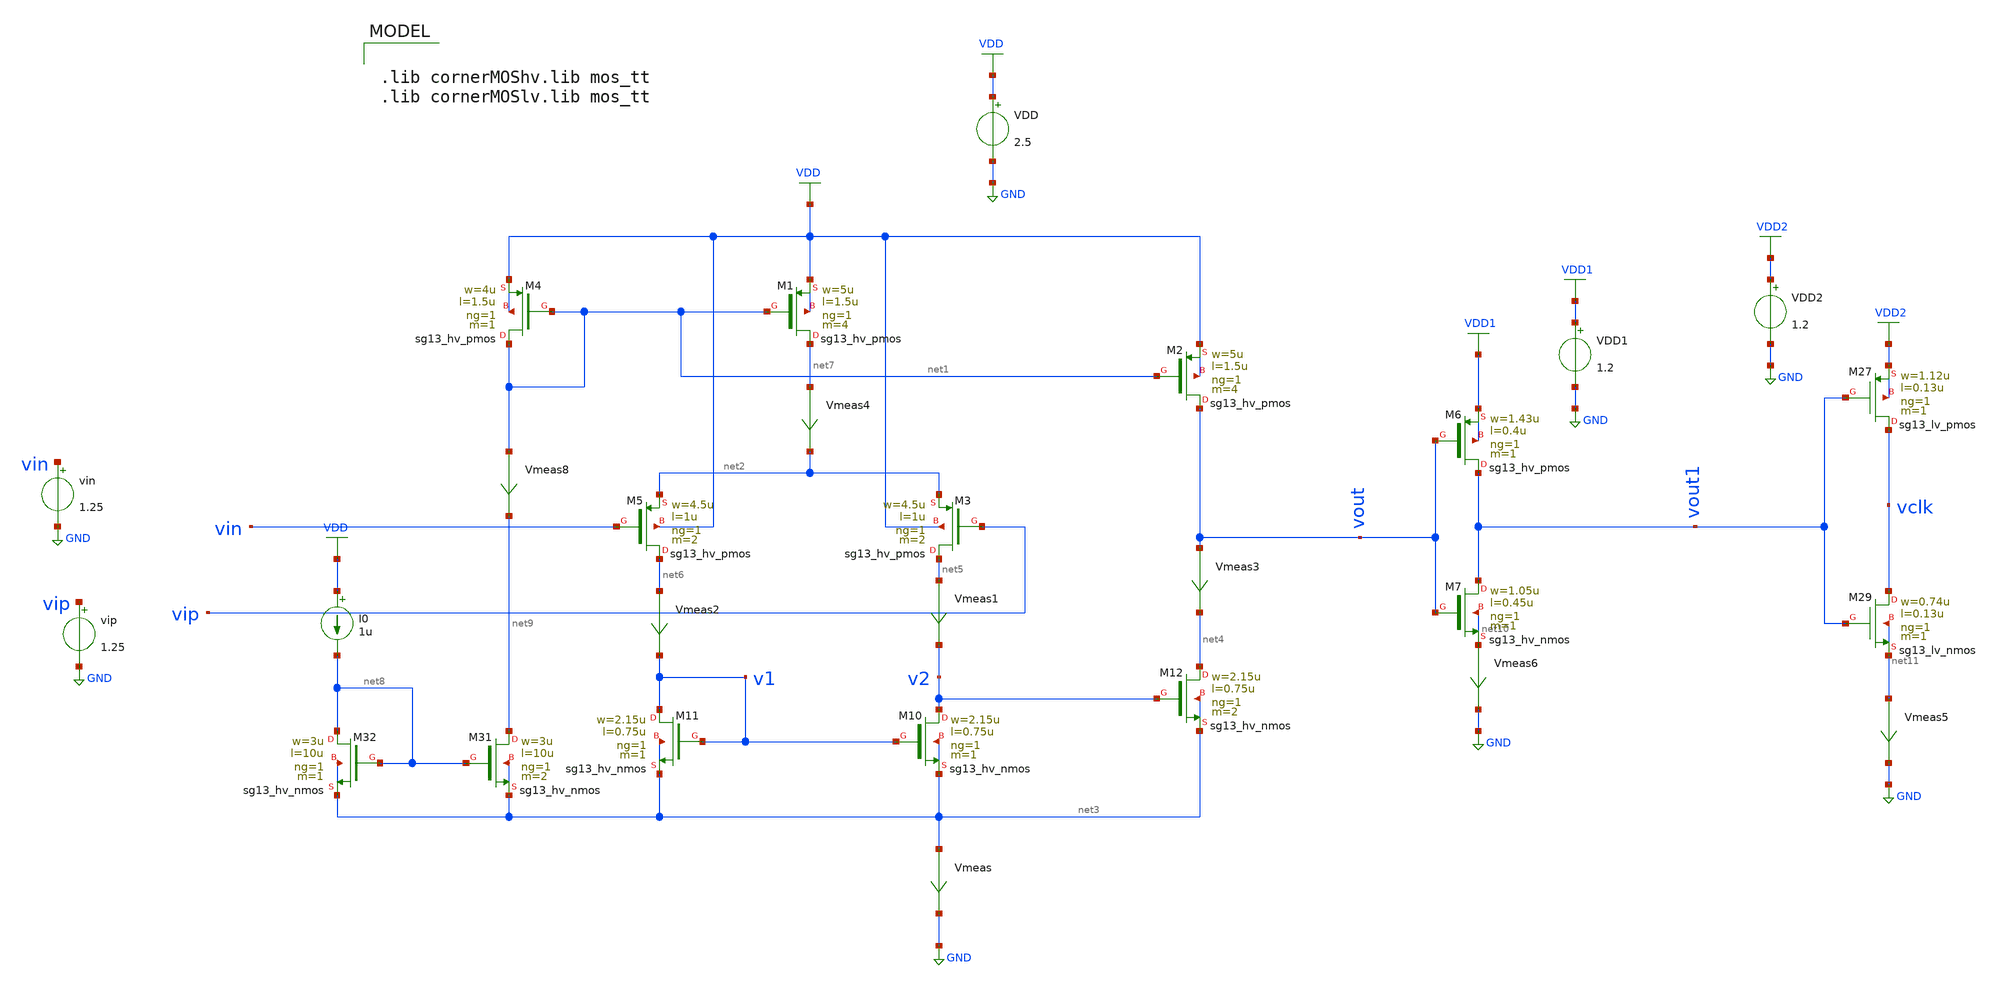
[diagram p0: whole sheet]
** sch_path: dependencies/ClockExtractor/ClockExtractor-main/schematic/xschem/schematic/clock_extraactor_op_2026.sch
**.subckt clock_extraactor_op_2026
VDD VDD GND 2.5
VDD1 VDD1 GND 1.2
XM7 vout1 vout net10 net10 sg13_hv_nmos w=1.05u l=0.45u ng=1 m=1 mm_ok=1
XM6 vout1 vout VDD1 VDD1 sg13_hv_pmos w=1.43u l=0.4u ng=1 m=1 mm_ok=1
Vmeas6 net10 GND 0
.save i(vmeas6)
XM4 net1 net1 VDD VDD sg13_hv_pmos w=4u l=1.5u ng=1 m=1 mm_ok=1
XM1 net7 net1 VDD VDD sg13_hv_pmos w=5u l=1.5u ng=1 m=4 mm_ok=1
XM2 vout net1 VDD VDD sg13_hv_pmos w=5u l=1.5u ng=1 m=4 mm_ok=1
XM3 net5 vip net2 VDD sg13_hv_pmos w=4.5u l=1u ng=1 m=2 mm_ok=1
XM5 net6 vin net2 VDD sg13_hv_pmos w=4.5u l=1u ng=1 m=2 mm_ok=1
XM10 v2 v1 net3 net3 sg13_hv_nmos w=2.15u l=0.75u ng=1 m=1 mm_ok=1
XM11 v1 v1 net3 net3 sg13_hv_nmos w=2.15u l=0.75u ng=1 m=1 mm_ok=1
XM12 net4 v2 net3 net3 sg13_hv_nmos w=2.15u l=0.75u ng=1 m=2 mm_ok=1
Vmeas net3 GND 0
.save i(vmeas)
Vmeas1 net5 v2 0
.save i(vmeas1)
Vmeas2 net6 v1 0
.save i(vmeas2)
Vmeas3 vout net4 0
.save i(vmeas3)
Vmeas4 net7 net2 0
.save i(vmeas4)
Vmeas5 net11 GND 0
.save i(vmeas5)
XM27 vclk vout1 VDD2 VDD2 sg13_lv_pmos w=1.12u l=0.13u ng=1 m=1 mm_ok=1
XM29 vclk vout1 net11 net11 sg13_lv_nmos w=0.74u l=0.13u ng=1 m=1 mm_ok=1
VDD2 VDD2 GND 1.2
XM31 net9 net8 net3 net3 sg13_hv_nmos w=3u l=10u ng=1 m=2 mm_ok=1
XM32 net8 net8 net3 net3 sg13_hv_nmos w=3u l=10u ng=1 m=1 mm_ok=1
Vmeas8 net1 net9 0
.save i(vmeas8)
I0 VDD net8 1u
vin vin GND 1.25
vip vip GND 1.25
**** begin user architecture code

.lib cornerMOShv.lib mos_tt
.lib cornerMOSlv.lib mos_tt



.param temp=27
//.include clock_extraactor_op_2026.save
//.save all
//.save @n.xm1.nsg13_hv_pmos
.control
save all
op

save @n.xm1.nsg13_hv_pmos[gm]
save @n.xm1.nsg13_hv_pmos[vds]
save @n.xm1.nsg13_hv_pmos[vth]
save @n.xm1.nsg13_hv_pmos[vgs]
save @n.xm1.nsg13_hv_pmos[ids]
save @n.xm1.nsg13_hv_pmos[gds]
save @n.xm1.nsg13_hv_pmos[cgg]
save @n.xm1.nsg13_hv_pmos[cgd]
save @n.xm1.nsg13_hv_pmos[vsat]

print @n.xm1.nsg13_hv_pmos[ids]
print @n.xm1.nsg13_hv_pmos[gds]
print @n.xm1.nsg13_hv_pmos[gm]
print @n.xm1.nsg13_hv_pmos[vds]
print @n.xm1.nsg13_hv_pmos[vth]
print @n.xm1.nsg13_hv_pmos[vsat]
print @n.xm1.nsg13_hv_pmos[vgs]
print @n.xm1.nsg13_hv_pmos[cgg]
print @n.xm1.nsg13_hv_pmos[cgd]

save @n.xm4.nsg13_hv_pmos[gm]
save @n.xm4.nsg13_hv_pmos[vds]
save @n.xm4.nsg13_hv_pmos[vgs]
save @n.xm4.nsg13_hv_pmos[vth]
save @n.xm4.nsg13_hv_pmos[ids]
save @n.xm4.nsg13_hv_pmos[gds]
save @n.xm4.nsg13_hv_pmos[cgg]
save @n.xm4.nsg13_hv_pmos[vsat]
save @n.xm4.nsg13_hv_pmos[cgd]

print @n.xm4.nsg13_hv_pmos[ids]
print @n.xm4.nsg13_hv_pmos[gds]
print @n.xm4.nsg13_hv_pmos[gm]
print @n.xm4.nsg13_hv_pmos[vds]
print @n.xm4.nsg13_hv_pmos[vth]
print @n.xm4.nsg13_hv_pmos[vsat]
print @n.xm4.nsg13_hv_pmos[vgs]
print @n.xm4.nsg13_hv_pmos[cgg]
print @n.xm4.nsg13_hv_pmos[cgd]

save @n.xm2.nsg13_hv_pmos[gm]
save @n.xm2.nsg13_hv_pmos[vdss]
save @n.xm2.nsg13_hv_pmos[vgs]
save @n.xm2.nsg13_hv_pmos[vth]
save @n.xm2.nsg13_hv_pmos[ids]
save @n.xm2.nsg13_hv_pmos[gds]
save @n.xm2.nsg13_hv_pmos[cgg]
save @n.xm2.nsg13_hv_pmos[vsat]
save @n.xm2.nsg13_hv_pmos[cgd]

print @n.xm2.nsg13_hv_pmos[ids]
print @n.xm2.nsg13_hv_pmos[gds]
print @n.xm2.nsg13_hv_pmos[gm]
print @n.xm2.nsg13_hv_pmos[vds]
print @n.xm2.nsg13_hv_pmos[vth]
print @n.xm2.nsg13_hv_pmos[vsat]
print @n.xm2.nsg13_hv_pmos[vgs]
print @n.xm2.nsg13_hv_pmos[cgg]
print @n.xm2.nsg13_hv_pmos[cgd]


save @n.xm5.nsg13_hv_pmos[gm]
save @n.xm5.nsg13_hv_pmos[vds]
save @n.xm5.nsg13_hv_pmos[vth]
save @n.xm5.nsg13_hv_pmos[vgs]
save @n.xm5.nsg13_hv_pmos[ids]
save @n.xm5.nsg13_hv_pmos[gds]
save @n.xm5.nsg13_hv_pmos[cgg]
save @n.xm5.nsg13_hv_pmos[cgd]
save @n.xm5.nsg13_hv_pmos[vsat]

print @n.xm5.nsg13_hv_pmos[ids]
print @n.xm5.nsg13_hv_pmos[gds]
print @n.xm5.nsg13_hv_pmos[gm]
print @n.xm5.nsg13_hv_pmos[vds]
print @n.xm5.nsg13_hv_pmos[vth]
print @n.xm5.nsg13_hv_pmos[vsat]
print @n.xm5.nsg13_hv_pmos[vgs]
print @n.xm5.nsg13_hv_pmos[cgg]
print @n.xm5.nsg13_hv_pmos[cgd]

save @n.xm11.nsg13_hv_nmos[gm]
save @n.xm11.nsg13_hv_nmos[vds]
save @n.xm11.nsg13_hv_nmos[vgs]
save @n.xm11.nsg13_hv_nmos[vth]
save @n.xm11.nsg13_hv_nmos[ids]
save @n.xm11.nsg13_hv_nmos[gds]
save @n.xm11.nsg13_hv_nmos[cgg]
save @n.xm11.nsg13_hv_nmos[vsat]
save @n.xm11.nsg13_hv_nmos[cgd]

print @n.xm11.nsg13_hv_nmos[ids]
print @n.xm11.nsg13_hv_nmos[gds]
print @n.xm11.nsg13_hv_nmos[gm]
print @n.xm11.nsg13_hv_nmos[vds]
print @n.xm11.nsg13_hv_nmos[vth]
print @n.xm11.nsg13_hv_nmos[vsat]
print @n.xm11.nsg13_hv_nmos[vgs]
print @n.xm11.nsg13_hv_nmos[cgg]
print @n.xm11.nsg13_hv_nmos[cgd]

save @n.xm12.nsg13_hv_nmos[gm]
save @n.xm12.nsg13_hv_nmos[vds]
save @n.xm12.nsg13_hv_nmos[vgs]
save @n.xm12.nsg13_hv_nmos[vth]
save @n.xm12.nsg13_hv_nmos[ids]
save @n.xm12.nsg13_hv_nmos[gds]
save @n.xm12.nsg13_hv_nmos[cgg]
save @n.xm12.nsg13_hv_nmos[vsat]
save @n.xm12.nsg13_hv_nmos[cgd]

print @n.xm12.nsg13_hv_nmos[ids]
print @n.xm12.nsg13_hv_nmos[gds]
print @n.xm12.nsg13_hv_nmos[gm]
print @n.xm12.nsg13_hv_nmos[vds]
print @n.xm12.nsg13_hv_nmos[vth]
print @n.xm12.nsg13_hv_nmos[vsat]
print @n.xm12.nsg13_hv_nmos[vgs]
print @n.xm12.nsg13_hv_nmos[cgg]
print @n.xm12.nsg13_hv_nmos[cgd]

save @n.xm6.nsg13_hv_pmos[gm]
save @n.xm6.nsg13_hv_pmos[vds]
save @n.xm6.nsg13_hv_pmos[vgs]
save @n.xm6.nsg13_hv_pmos[vth]
save @n.xm6.nsg13_hv_pmos[ids]
save @n.xm6.nsg13_hv_pmos[gds]
save @n.xm6.nsg13_hv_pmos[cgg]
save @n.xm6.nsg13_hv_pmos[vsat]
save @n.xm6.nsg13_hv_pmos[cgd]

print @n.xm6.nsg13_hv_pmos[ids]
print @n.xm6.nsg13_hv_pmos[gds]
print @n.xm6.nsg13_hv_pmos[gm]
print @n.xm6.nsg13_hv_pmos[vds]
print @n.xm6.nsg13_hv_pmos[vth]
print @n.xm6.nsg13_hv_pmos[vsat]
print @n.xm6.nsg13_hv_pmos[vgs]
print @n.xm6.nsg13_hv_pmos[cgg]
print @n.xm6.nsg13_hv_pmos[cgd]


save @n.xm7.nsg13_hv_nmos[gm]
save @n.xm7.nsg13_hv_nmos[vds]
save @n.xm7.nsg13_hv_nmos[vgs]
save @n.xm7.nsg13_hv_nmos[vth]
save @n.xm7.nsg13_hv_nmos[ids]
save @n.xm7.nsg13_hv_nmos[gds]
save @n.xm7.nsg13_hv_nmos[cgg]
save @n.xm7.nsg13_hv_nmos[vsat]
save @n.xm7.nsg13_hv_nmos[cgd]

print @n.xm7.nsg13_hv_nmos[ids]
print @n.xm7.nsg13_hv_nmos[gds]
print @n.xm7.nsg13_hv_nmos[gm]
print @n.xm7.nsg13_hv_nmos[vds]
print @n.xm7.nsg13_hv_nmos[vth]
print @n.xm7.nsg13_hv_nmos[vsat]
print @n.xm7.nsg13_hv_nmos[vgs]
print @n.xm7.nsg13_hv_nmos[cgg]
print @n.xm7.nsg13_hv_nmos[cgd]

save @n.xm29.nsg13_lv_nmos[gm]
save @n.xm29.nsg13_lv_nmos[vds]
save @n.xm29.nsg13_lv_nmos[vgs]
save @n.xm29.nsg13_lv_nmos[vth]
save @n.xm29.nsg13_lv_nmos[ids]
save @n.xm29.nsg13_lv_nmos[gds]
save @n.xm29.nsg13_lv_nmos[cgg]
save @n.xm29.nsg13_lv_nmos[cgd]
save @n.xm29.nsg13_lv_nmos[vsat]

print @n.xm29.nsg13_lv_nmos[ids]
print @n.xm29.nsg13_lv_nmos[gds]
print @n.xm29.nsg13_lv_nmos[gm]
print @n.xm29.nsg13_lv_nmos[vds]
print @n.xm29.nsg13_lv_nmos[vth]
print @n.xm29.nsg13_lv_nmos[vsat]
print @n.xm29.nsg13_lv_nmos[vgs]
print @n.xm29.nsg13_lv_nmos[cgg]
print @n.xm29.nsg13_lv_nmos[cgd]

save @n.xm27.nsg13_lv_pmos[gm]
save @n.xm27.nsg13_lv_pmos[vds]
save @n.xm27.nsg13_lv_pmos[vgs]
save @n.xm27.nsg13_lv_pmos[vth]
save @n.xm27.nsg13_lv_pmos[ids]
save @n.xm27.nsg13_lv_pmos[gds]
save @n.xm27.nsg13_lv_pmos[cgg]
save @n.xm27.nsg13_lv_pmos[cgd]
save @n.xm27.nsg13_lv_pmos[vsat]

print @n.xm27.nsg13_lv_pmos[ids]
print @n.xm27.nsg13_lv_pmos[gds]
print @n.xm27.nsg13_lv_pmos[gm]
print @n.xm27.nsg13_lv_pmos[vds]
print @n.xm27.nsg13_lv_pmos[vth]
print @n.xm27.nsg13_lv_pmos[vsat]
print @n.xm27.nsg13_lv_pmos[vgs]
print @n.xm27.nsg13_lv_pmos[cgg]
print @n.xm27.nsg13_lv_pmos[cgd]

write clock_extraactor_op_2026.raw
.endc


**** end user architecture code
**.ends
.GLOBAL GND
.GLOBAL VDD
.GLOBAL VDD1
.GLOBAL VDD2
.end
